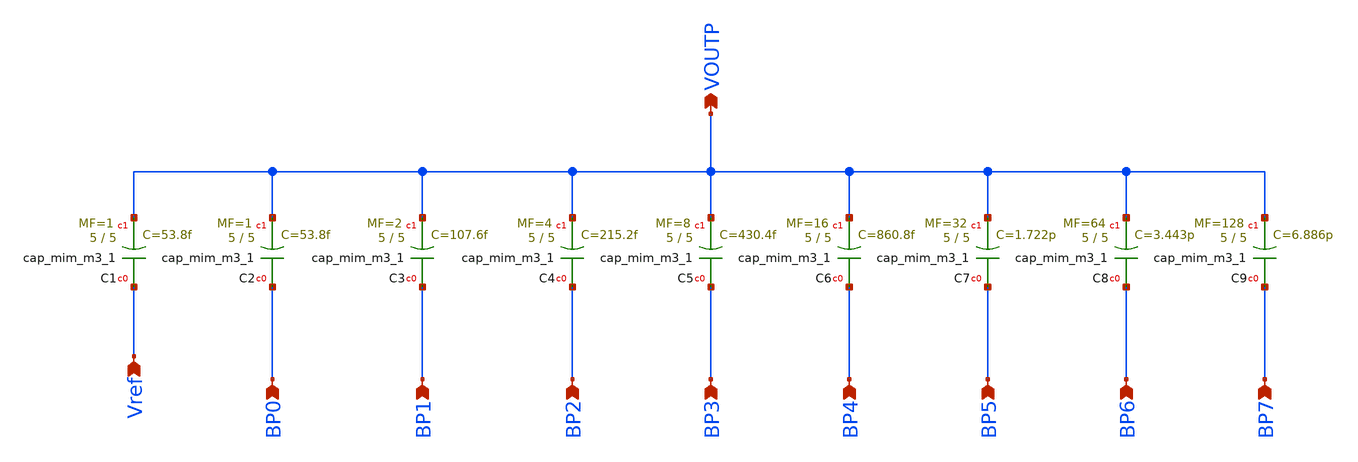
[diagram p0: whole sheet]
** sch_path: 05_mixed_signal/soluzioni/lab03/xschem/cdac.sch
**.subckt cdac Vref VOUTP BP0 BP1 BP2 BP3 BP4 BP5 BP6 BP7
*.ipin Vref
*.opin VOUTP
*.ipin BP0
*.ipin BP1
*.ipin BP2
*.ipin BP3
*.ipin BP4
*.ipin BP5
*.ipin BP6
*.ipin BP7
XC1 Vref VOUTP sky130_fd_pr__cap_mim_m3_1 W=5 L=5 MF=1 m=1
XC2 BP0 VOUTP sky130_fd_pr__cap_mim_m3_1 W=5 L=5 MF=1 m=1
XC3 BP1 VOUTP sky130_fd_pr__cap_mim_m3_1 W=5 L=5 MF=2 m=2
XC4 BP2 VOUTP sky130_fd_pr__cap_mim_m3_1 W=5 L=5 MF=4 m=4
XC5 BP3 VOUTP sky130_fd_pr__cap_mim_m3_1 W=5 L=5 MF=8 m=8
XC6 BP4 VOUTP sky130_fd_pr__cap_mim_m3_1 W=5 L=5 MF=16 m=16
XC7 BP5 VOUTP sky130_fd_pr__cap_mim_m3_1 W=5 L=5 MF=32 m=32
XC8 BP6 VOUTP sky130_fd_pr__cap_mim_m3_1 W=5 L=5 MF=64 m=64
XC9 BP7 VOUTP sky130_fd_pr__cap_mim_m3_1 W=5 L=5 MF=128 m=128
**.ends
.end
